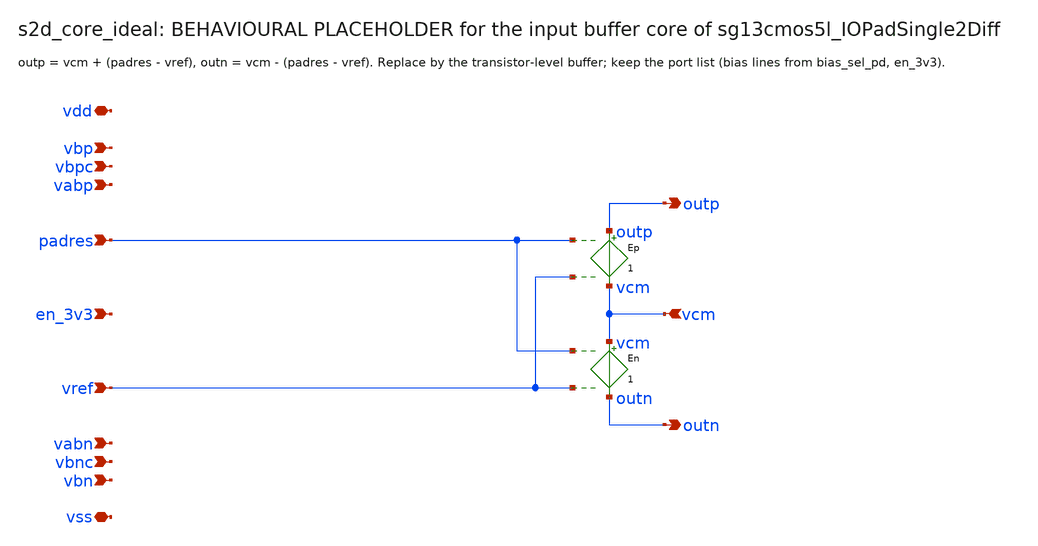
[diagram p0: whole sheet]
** sch_path: macros/sg13cmos5l_IOPadSingle2Diff/schematic/xschem/s2d_core_ideal.sch
**.subckt s2d_core_ideal vdd vss padres vref vcm outp outn vbp vbn vbpc vbnc vabp vabn en_3v3
*.iopin vdd
*.iopin vss
*.ipin padres
*.ipin vref
*.ipin vcm
*.opin outp
*.opin outn
*.ipin vbp
*.ipin vbn
*.ipin vbpc
*.ipin vbnc
*.ipin vabp
*.ipin vabn
*.ipin en_3v3
Ep outp vcm padres vref 1
En vcm outn padres vref 1
**.ends
.end
